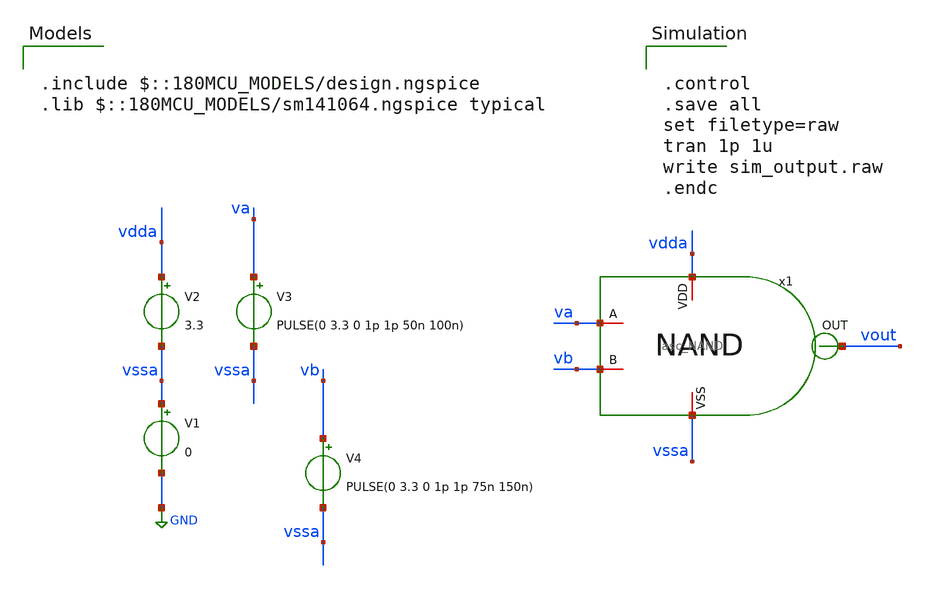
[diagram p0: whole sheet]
** sch_path: designs/libs/xp_tb_analog/tb_asc_NAND/tb_asc_NAND.sch
**.subckt tb_asc_NAND
V1 vssa GND 0
V2 vdda vssa 3.3
V3 va vssa PULSE(0 3.3 0 1p 1p 50n 100n)
x1 vdda vout va vb vssa asc_NAND
V4 vb vssa PULSE(0 3.3 0 1p 1p 75n 150n)
**** begin user architecture code

.include $::180MCU_MODELS/design.ngspice
.lib $::180MCU_MODELS/sm141064.ngspice typical



.control
.save all
set filetype=raw
tran 1p 1u
write sim_output.raw
.endc


**** end user architecture code
**.ends

* expanding   symbol:  libs/core_analog/asc_NAND/asc_NAND.sym # of pins=5
** sym_path: designs/libs/xp_core_analog/asc_NAND/asc_NAND.sym
** sch_path: designs/libs/xp_core_analog/asc_NAND/asc_NAND.sch
.subckt asc_NAND VDD OUT A B VSS
*.iopin VDD
*.iopin VSS
*.iopin B
*.iopin A
*.iopin OUT
XM1 OUT A net1 VSS nfet_03v3 L=0.5u W=2u nf=1 ad='int((nf+1)/2) * W/nf * 0.18u' as='int((nf+2)/2) * W/nf * 0.18u'
+ pd='2*int((nf+1)/2) * (W/nf + 0.18u)' ps='2*int((nf+2)/2) * (W/nf + 0.18u)' nrd='0.18u / W' nrs='0.18u / W'
+ sa=0 sb=0 sd=0 m=1
XM2 OUT A VDD VDD pfet_03v3 L=0.5u W=3u nf=1 ad='int((nf+1)/2) * W/nf * 0.18u' as='int((nf+2)/2) * W/nf * 0.18u'
+ pd='2*int((nf+1)/2) * (W/nf + 0.18u)' ps='2*int((nf+2)/2) * (W/nf + 0.18u)' nrd='0.18u / W' nrs='0.18u / W'
+ sa=0 sb=0 sd=0 m=1
XM3 net1 B VSS VSS nfet_03v3 L=0.5u W=2u nf=1 ad='int((nf+1)/2) * W/nf * 0.18u' as='int((nf+2)/2) * W/nf * 0.18u'
+ pd='2*int((nf+1)/2) * (W/nf + 0.18u)' ps='2*int((nf+2)/2) * (W/nf + 0.18u)' nrd='0.18u / W' nrs='0.18u / W'
+ sa=0 sb=0 sd=0 m=1
XM4 OUT B VDD VDD pfet_03v3 L=0.5u W=3u nf=1 ad='int((nf+1)/2) * W/nf * 0.18u' as='int((nf+2)/2) * W/nf * 0.18u'
+ pd='2*int((nf+1)/2) * (W/nf + 0.18u)' ps='2*int((nf+2)/2) * (W/nf + 0.18u)' nrd='0.18u / W' nrs='0.18u / W'
+ sa=0 sb=0 sd=0 m=1
.ends

.GLOBAL GND
.end
